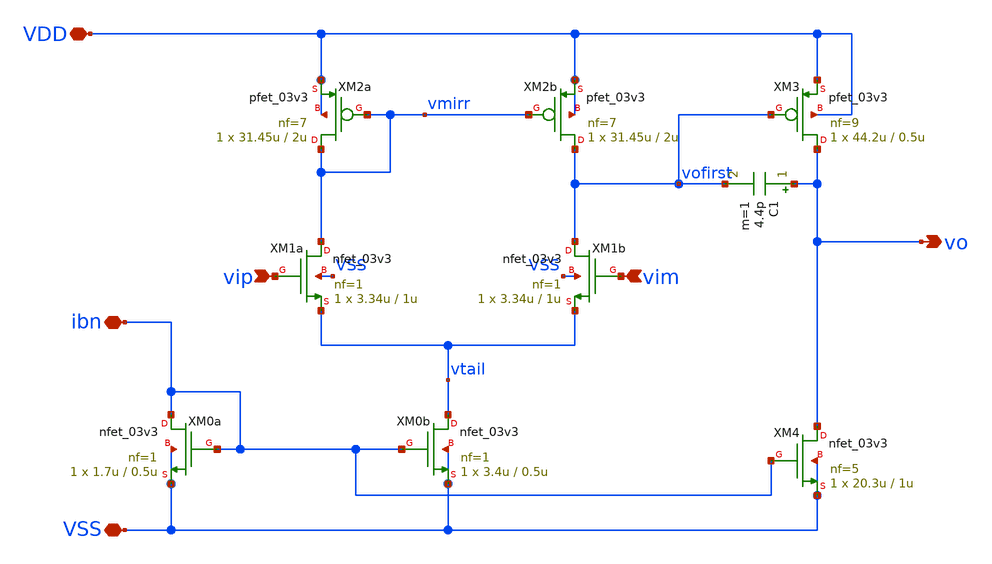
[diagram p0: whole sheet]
** sch_path: DESIGN/DACFUTURE_EDU/Two_stage_OTA/two_stage_ota_nmos.sch
**.subckt two_stage_ota_nmos vip vim vo VDD VSS ibn
*.ipin vip
*.ipin vim
*.opin vo
*.iopin VDD
*.iopin VSS
*.iopin ibn
XM2b vofirst vmirr VDD VDD pfet_03v3 L=2u W=31.45u nf=7 ad='int((nf+1)/2) * W/nf * 0.18u' as='int((nf+2)/2) * W/nf * 0.18u'
+ pd='2*int((nf+1)/2) * (W/nf + 0.18u)' ps='2*int((nf+2)/2) * (W/nf + 0.18u)' nrd='0.18u / W' nrs='0.18u / W'
+ sa=0 sb=0 sd=0 m=1
XM2a vmirr vmirr VDD VDD pfet_03v3 L=2u W=31.45u nf=7 ad='int((nf+1)/2) * W/nf * 0.18u' as='int((nf+2)/2) * W/nf * 0.18u'
+ pd='2*int((nf+1)/2) * (W/nf + 0.18u)' ps='2*int((nf+2)/2) * (W/nf + 0.18u)' nrd='0.18u / W' nrs='0.18u / W'
+ sa=0 sb=0 sd=0 m=1
XM1a vmirr vip vtail VSS nfet_03v3 L=1u W=3.34u nf=1 ad='int((nf+1)/2) * W/nf * 0.18u' as='int((nf+2)/2) * W/nf * 0.18u'
+ pd='2*int((nf+1)/2) * (W/nf + 0.18u)' ps='2*int((nf+2)/2) * (W/nf + 0.18u)' nrd='0.18u / W' nrs='0.18u / W'
+ sa=0 sb=0 sd=0 m=1
XM0b vtail ibn VSS VSS nfet_03v3 L=0.5u W=3.4u nf=1 ad='int((nf+1)/2) * W/nf * 0.18u' as='int((nf+2)/2) * W/nf * 0.18u'
+ pd='2*int((nf+1)/2) * (W/nf + 0.18u)' ps='2*int((nf+2)/2) * (W/nf + 0.18u)' nrd='0.18u / W' nrs='0.18u / W'
+ sa=0 sb=0 sd=0 m=1
XM1b vofirst vim vtail VSS nfet_03v3 L=1u W=3.34u nf=1 ad='int((nf+1)/2) * W/nf * 0.18u' as='int((nf+2)/2) * W/nf * 0.18u'
+ pd='2*int((nf+1)/2) * (W/nf + 0.18u)' ps='2*int((nf+2)/2) * (W/nf + 0.18u)' nrd='0.18u / W' nrs='0.18u / W'
+ sa=0 sb=0 sd=0 m=1
XM0a ibn ibn VSS VSS nfet_03v3 L=0.5u W=1.7u nf=1 ad='int((nf+1)/2) * W/nf * 0.18u' as='int((nf+2)/2) * W/nf * 0.18u'
+ pd='2*int((nf+1)/2) * (W/nf + 0.18u)' ps='2*int((nf+2)/2) * (W/nf + 0.18u)' nrd='0.18u / W' nrs='0.18u / W'
+ sa=0 sb=0 sd=0 m=1
XM4 vo ibn VSS VSS nfet_03v3 L=1u W=20.3u nf=5 ad='int((nf+1)/2) * W/nf * 0.18u' as='int((nf+2)/2) * W/nf * 0.18u'
+ pd='2*int((nf+1)/2) * (W/nf + 0.18u)' ps='2*int((nf+2)/2) * (W/nf + 0.18u)' nrd='0.18u / W' nrs='0.18u / W'
+ sa=0 sb=0 sd=0 m=1
XM3 vo vofirst VDD VDD pfet_03v3 L=0.5u W=44.2u nf=9 ad='int((nf+1)/2) * W/nf * 0.18u' as='int((nf+2)/2) * W/nf * 0.18u'
+ pd='2*int((nf+1)/2) * (W/nf + 0.18u)' ps='2*int((nf+2)/2) * (W/nf + 0.18u)' nrd='0.18u / W' nrs='0.18u / W'
+ sa=0 sb=0 sd=0 m=1
C1 vo vofirst 4.4p m=1
**.ends
.end
